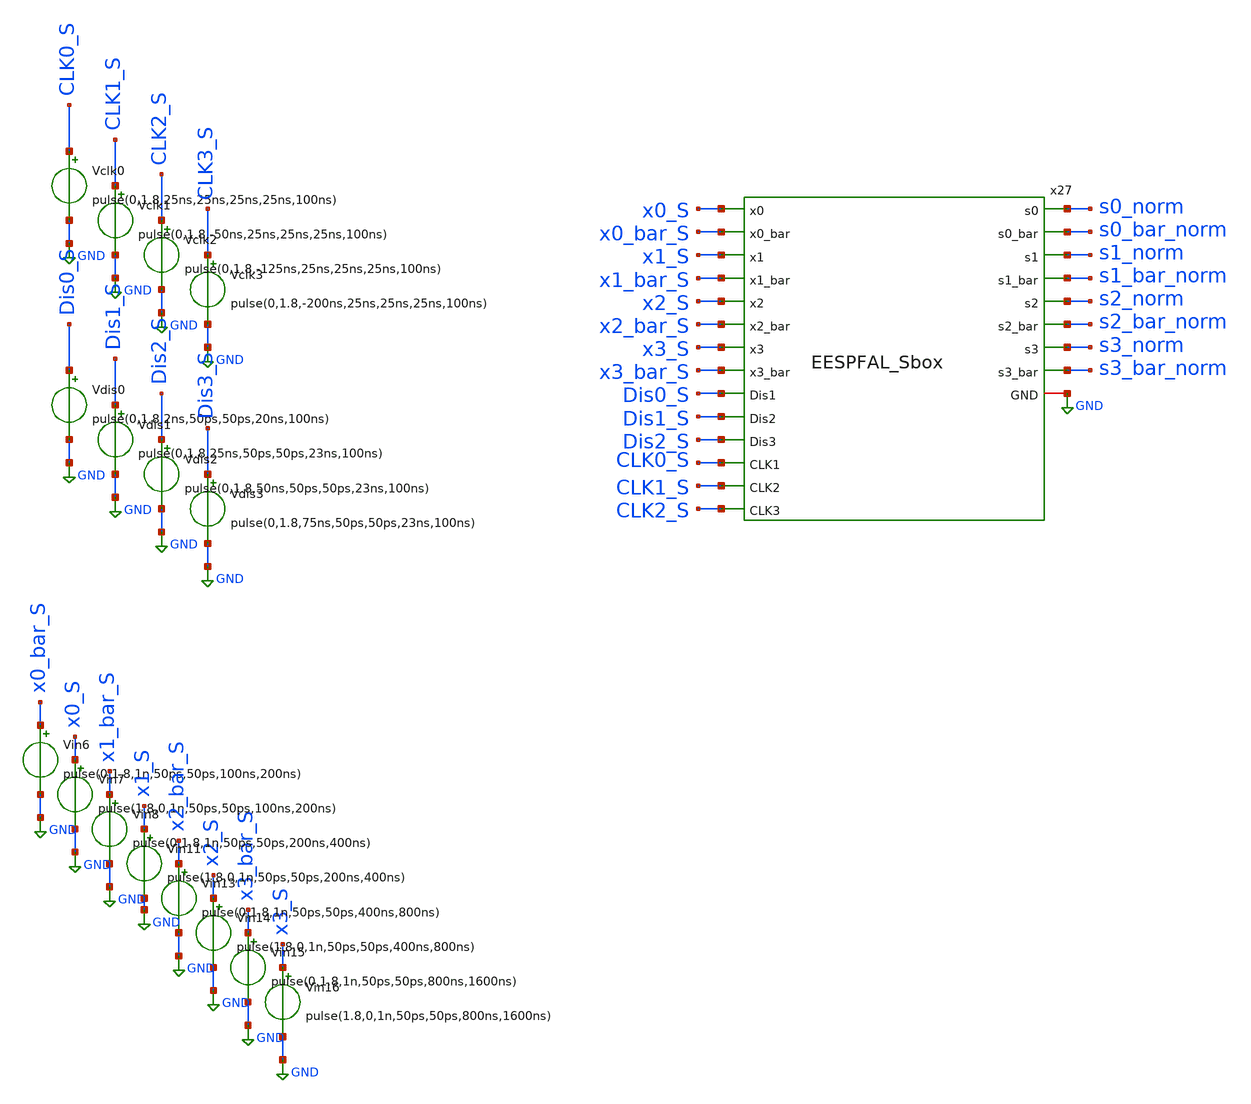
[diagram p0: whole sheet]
** sch_path: skywater_stuff/EESPFAL_sbox_sim.sch
**.subckt EESPFAL_sbox_sim
Vdis0 Dis0_S GND pulse(0,1.8,2ns,50ps,50ps,20ns,100ns)
Vclk0 CLK0_S GND pulse(0,1.8,25ns,25ns,25ns,25ns,100ns)
Vdis1 Dis1_S GND pulse(0,1.8,25ns,50ps,50ps,23ns,100ns)
Vdis2 Dis2_S GND pulse(0,1.8,50ns,50ps,50ps,23ns,100ns)
Vdis3 Dis3_S GND pulse(0,1.8,75ns,50ps,50ps,23ns,100ns)
Vclk1 CLK1_S GND pulse(0,1.8,-50ns,25ns,25ns,25ns,100ns)
Vclk2 CLK2_S GND pulse(0,1.8,-125ns,25ns,25ns,25ns,100ns)
Vclk3 CLK3_S GND pulse(0,1.8,-200ns,25ns,25ns,25ns,100ns)
x27 GND x0_S x0_bar_S x1_S x1_bar_S x2_S x2_bar_S x3_S x3_bar_S Dis0_S CLK0_S CLK1_S Dis1_S CLK2_S
+ Dis2_S s0_norm s0_bar_norm s1_bar_norm s1_norm s2_norm s2_bar_norm s3_bar_norm s3_norm EESPFAL_Sbox
Vin6 x0_bar_S GND pulse(0,1.8,1n,50ps,50ps,100ns,200ns)
Vin7 x0_S GND pulse(1.8,0,1n,50ps,50ps,100ns,200ns)
Vin8 x1_bar_S GND pulse(0,1.8,1n,50ps,50ps,200ns,400ns)
Vin11 x1_S GND pulse(1.8,0,1n,50ps,50ps,200ns,400ns)
Vin13 x2_bar_S GND pulse(0,1.8,1n,50ps,50ps,400ns,800ns)
Vin14 x2_S GND pulse(1.8,0,1n,50ps,50ps,400ns,800ns)
Vin15 x3_bar_S GND pulse(0,1.8,1n,50ps,50ps,800ns,1600ns)
Vin16 x3_S GND pulse(1.8,0,1n,50ps,50ps,800ns,1600ns)
**** begin user architecture code

.lib /research/pdk/open_pdks/share/pdk/sky130A/libs.tech/ngspice/sky130.lib.spice tt
**.include ~/magic_layout_stuff/EESPFAL_Sbox.spice
**.include ~/magic_layout_stuff/EESPFAL_Sbox_flat.spice
.option method=gear
.control
save all
tran 0.01n 2u
plot v(s0_norm) v(s1_norm) v(s2_norm) v(s3_norm)
**plot v(s0_flat) v(s1_flat) v(s2_flat) v(s3_flat)
plot v(s0_norm)
plot v(s1_norm)
plot v(s2_norm)
plot v(s3_norm)
plot v(x0_S)
plot v(x1_S)
plot v(x2_S)
plot v(x3_S)
**plot v(s0_flat)
**plot v(s1_flat)
**plot v(s2_flat)
**plot v(s3_flat)
plot v(s0_bar_norm) v(s1_bar_norm) v(s2_bar_norm) v(s3_bar_norm)
**plot v(s0_bar_flat) v(s1_bar_flat) v(s2_bar_flat) v(s3_bar_flat)
let Pinst_CLK0_CLK2 = (v(CLK0_S)*i(vclk0))+(v(CLK1_S)*i(vclk1))+(v(CLK2_S)*i(vclk2))
plot Pinst_CLK0_CLK2
**let Pinst_CLK0_CLK2_Dis0_Dis2 =
*+ (v(CLK0)*i(vclk0))+(v(Dis0)*i(Vdis0))+(v(CLK1)*i(vclk1))+(v(Dis1)*i(Vdis1))+(v(CLK2)*i(vclk2))+(v(Dis2)*i(Vdis2))
**plot Pinst_CLK0
**plot Pinst_CLK1_CLK3
**plot Pinst_CLK0_CLK2_Dis0_Dis2
**wrdata EESPFAL_sbox.raw v(s0_norm) v(s1_norm) v(s2_norm) v(s3_norm) v(s0_bar_norm) v(s1_bar_norm)
*+ v(s2_bar_norm) v(s3_bar_norm)
**wrdata EESPFAL_sbox_PEX.raw v(s0_flat) v(s1_flat) v(s2_flat) v(s3_flat) v(s0_bar_flat)
*+ v(s1_bar_flat) v(s2_bar_flat) v(s3_bar_flat)
**wrdata EESPFAL_sbox.csv v(s0_norm) v(s1_norm) v(s2_norm) v(s3_norm) v(s0_bar_norm) v(s1_bar_norm)
*+ v(s2_bar_norm) v(s3_bar_norm)
**wrdata EESPFAL_sbox_PEX.csv v(s0_flat) v(s1_flat) v(s2_flat) v(s3_flat) v(s0_bar_flat)
*+ v(s1_bar_flat) v(s2_bar_flat) v(s3_bar_flat)
**wrdata EESPFAL_sbox_sim.raw Pinst_CLK1_CLK3
**wrdata EESPFAL_sbox_test.csv Pinst_CLK1_CLK3
**wrdata EESPFAL_sbox_PEX_sim.raw Pinst_CLK1_CLK3
wrdata EESPFAL_sbox_sim.csv Pinst_CLK0_CLK2
.endc


**** end user architecture code
**.ends
.GLOBAL GND
.end
